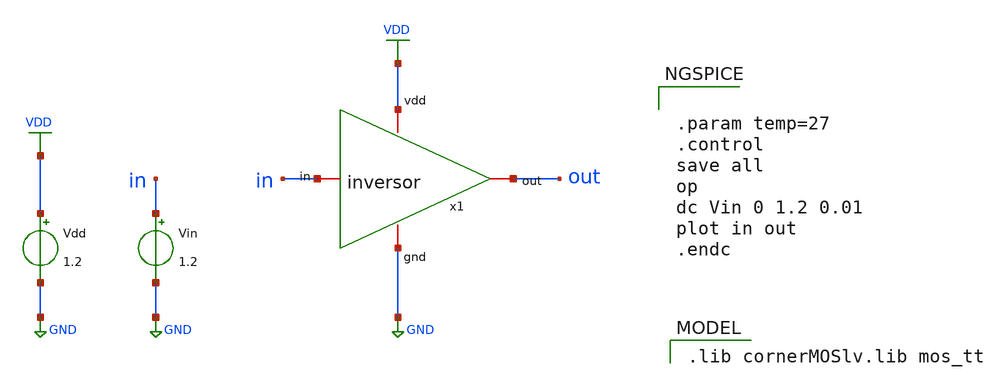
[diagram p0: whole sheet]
** sch_path: xschem/tb-inversor-dc.sch
**.subckt tb-inversor-dc
x1 VDD out in GND inversor
Vin in GND 1.2
Vdd VDD GND 1.2
**** begin user architecture code


.param temp=27
.control
save all
op
dc Vin 0 1.2 0.01
plot in out
.endc


 .lib cornerMOSlv.lib mos_tt

**** end user architecture code
**.ends

* expanding   symbol:  /home/edsonihp/ihp130_skel/tarefa1/inversor.sym # of pins=4
** sym_path: xschem/inversor.sym
** sch_path: xschem/inversor.sch
.subckt inversor vdd out in gnd
*.iopin out
*.iopin vdd
*.iopin gnd
*.iopin in
XM1 out in gnd gnd sg13_lv_nmos w=0.45u l=0.15u ng=1 m=1 mm_ok=1
XM2 out in vdd vdd sg13_lv_pmos w=0.9u l=0.15u ng=1 m=1 mm_ok=1
.ends

.GLOBAL GND
.GLOBAL VDD
.end
